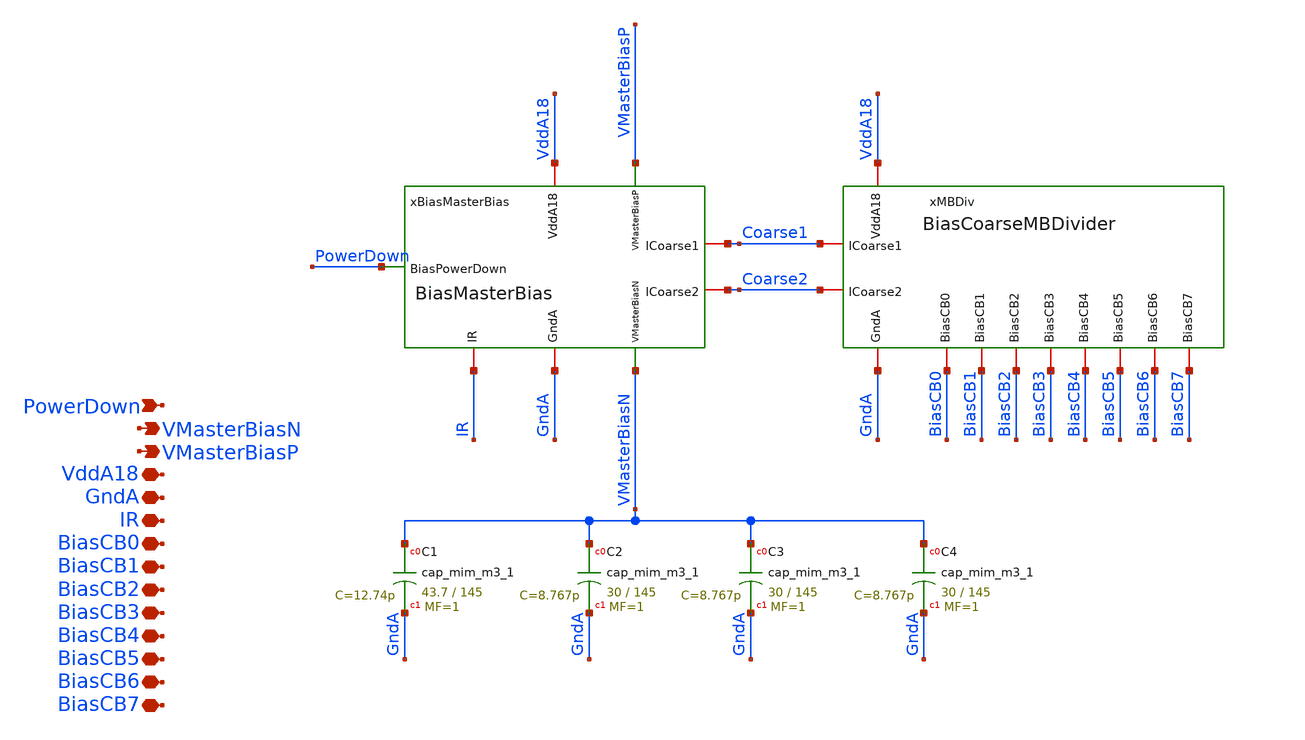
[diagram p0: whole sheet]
** sch_path: analog/xschem/BiasMasternCoarse_og.sch
**.subckt BiasMasternCoarse_og PowerDown VMasterBiasN VddA18 GndA IR VMasterBiasP BiasCB0 BiasCB1
*+ BiasCB2 BiasCB3 BiasCB4 BiasCB5 BiasCB6 BiasCB7
*.ipin PowerDown
*.opin VMasterBiasN
*.iopin VddA18
*.iopin GndA
*.iopin IR
*.opin VMasterBiasP
*.iopin BiasCB0
*.iopin BiasCB1
*.iopin BiasCB2
*.iopin BiasCB3
*.iopin BiasCB4
*.iopin BiasCB5
*.iopin BiasCB6
*.iopin BiasCB7
xBiasMasterBias VMasterBiasP Coarse2 Coarse1 VMasterBiasN PowerDown VddA18 GndA IR BiasMasterBias
xMBDiv VddA18 GndA Coarse2 Coarse1 BiasCB0 BiasCB1 BiasCB3 BiasCB4 BiasCB5 BiasCB6 BiasCB7 BiasCB2
+ BiasCoarseMBDivider
XC1 VMasterBiasN GndA sky130_fd_pr__cap_mim_m3_1 W=43.7 L=145 MF=1 m=1
XC2 VMasterBiasN GndA sky130_fd_pr__cap_mim_m3_1 W=30 L=145 MF=1 m=1
XC3 VMasterBiasN GndA sky130_fd_pr__cap_mim_m3_1 W=30 L=145 MF=1 m=1
XC4 VMasterBiasN GndA sky130_fd_pr__cap_mim_m3_1 W=30 L=145 MF=1 m=1
**.ends
.end
